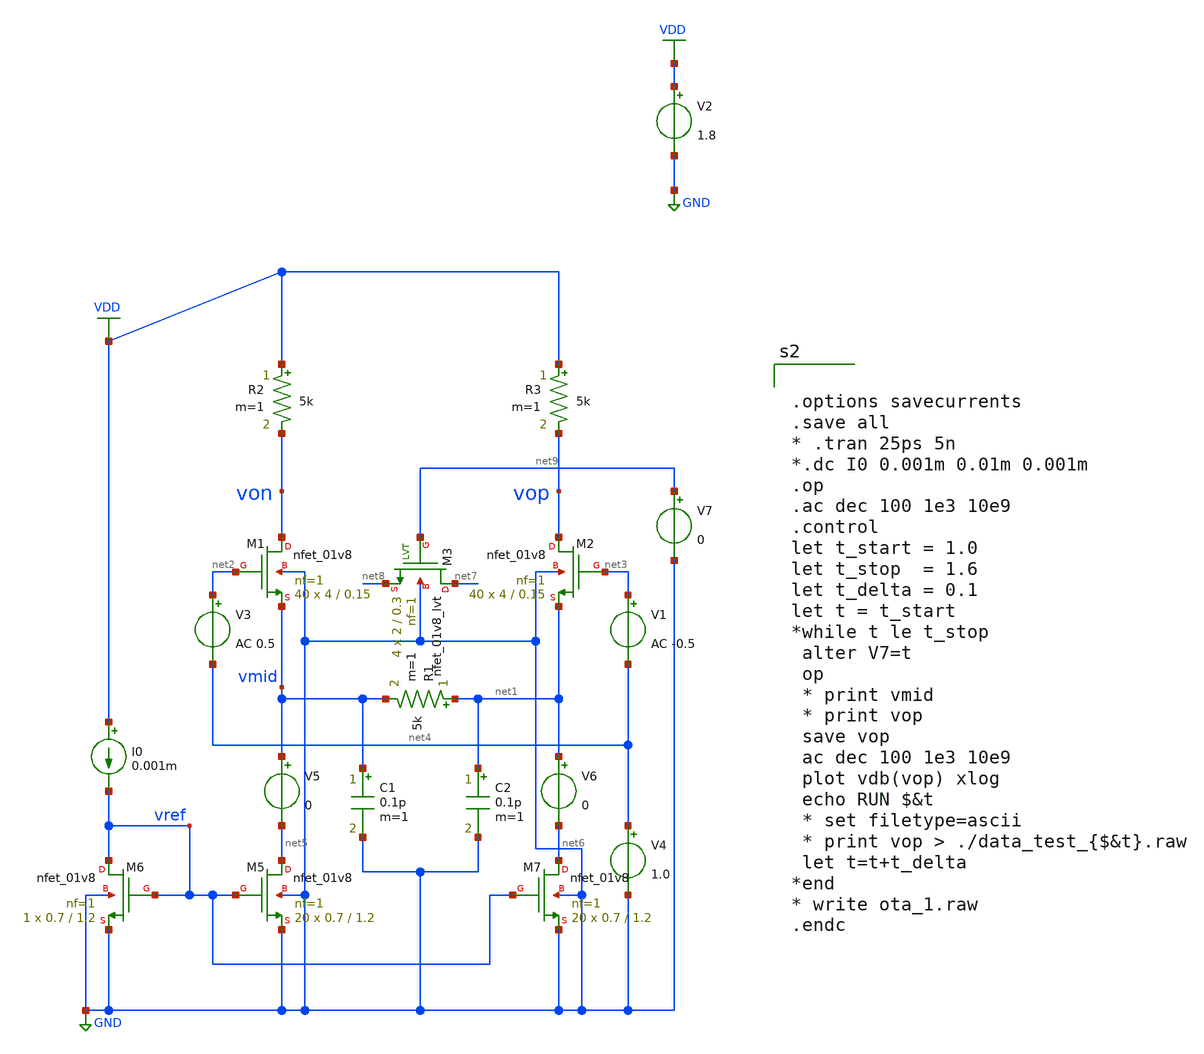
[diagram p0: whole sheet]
** sch_path: xschem/ctle_2.sch
**.subckt ctle_2
V2 VDD GND 1.8
XM5 net5 vref GND GND sky130_fd_pr__nfet_01v8 L=1.2 W=0.7 nf=1 ad='int((nf+1)/2) * W/nf * 0.29' as='int((nf+2)/2) * W/nf * 0.29'
+ pd='2*int((nf+1)/2) * (W/nf + 0.29)' ps='2*int((nf+2)/2) * (W/nf + 0.29)' nrd='0.29 / W' nrs='0.29 / W'
+ sa=0 sb=0 sd=0 mult=20 m=20
XM6 vref vref GND GND sky130_fd_pr__nfet_01v8 L=1.2 W=0.7 nf=1 ad='int((nf+1)/2) * W/nf * 0.29' as='int((nf+2)/2) * W/nf * 0.29'
+ pd='2*int((nf+1)/2) * (W/nf + 0.29)' ps='2*int((nf+2)/2) * (W/nf + 0.29)' nrd='0.29 / W' nrs='0.29 / W'
+ sa=0 sb=0 sd=0 mult=1 m=1
I0 VDD vref 0.001m
V3 net2 net4 AC 0.5
V4 net4 GND 1.0
V5 vmid net5 0
V1 net3 net4 AC -0.5
XM7 net6 vref GND GND sky130_fd_pr__nfet_01v8 L=1.2 W=0.7 nf=1 ad='int((nf+1)/2) * W/nf * 0.29' as='int((nf+2)/2) * W/nf * 0.29'
+ pd='2*int((nf+1)/2) * (W/nf + 0.29)' ps='2*int((nf+2)/2) * (W/nf + 0.29)' nrd='0.29 / W' nrs='0.29 / W'
+ sa=0 sb=0 sd=0 mult=20 m=20
V6 net1 net6 0
R1 net1 vmid 5k m=1
R2 VDD von 5k m=1
R3 VDD vop 5k m=1
C1 vmid GND 0.1p m=1
C2 net1 GND 0.1p m=1
XM3 net7 net9 net8 GND sky130_fd_pr__nfet_01v8_lvt L=0.3 W=2 nf=1 ad='int((nf+1)/2) * W/nf * 0.29' as='int((nf+2)/2) * W/nf * 0.29'
+ pd='2*int((nf+1)/2) * (W/nf + 0.29)' ps='2*int((nf+2)/2) * (W/nf + 0.29)' nrd='0.29 / W' nrs='0.29 / W'
+ sa=0 sb=0 sd=0 mult=4 m=4
V7 net9 GND 0
XM1 von net2 vmid GND sky130_fd_pr__nfet_01v8 L=0.15 W=4 nf=1 ad='int((nf+1)/2) * W/nf * 0.29' as='int((nf+2)/2) * W/nf * 0.29'
+ pd='2*int((nf+1)/2) * (W/nf + 0.29)' ps='2*int((nf+2)/2) * (W/nf + 0.29)' nrd='0.29 / W' nrs='0.29 / W'
+ sa=0 sb=0 sd=0 mult=40 m=40
XM2 vop net3 net1 GND sky130_fd_pr__nfet_01v8 L=0.15 W=4 nf=1 ad='int((nf+1)/2) * W/nf * 0.29' as='int((nf+2)/2) * W/nf * 0.29'
+ pd='2*int((nf+1)/2) * (W/nf + 0.29)' ps='2*int((nf+2)/2) * (W/nf + 0.29)' nrd='0.29 / W' nrs='0.29 / W'
+ sa=0 sb=0 sd=0 mult=40 m=40
**** begin user architecture code
.lib $::SKYWATER_MODELS/sky130.lib.spice tt
* .include $::PDKPATH/libs.ref/sky130_fd_sc_hvl/spice/sky130_fd_sc_hvl.spice



.options savecurrents
.save all
* .tran 25ps 5n
*.dc I0 0.001m 0.01m 0.001m
.op
.ac dec 100 1e3 10e9
.control
let t_start = 1.0
let t_stop  = 1.6
let t_delta = 0.1
let t = t_start
*while t le t_stop
 alter V7=t
 op
 * print vmid
 * print vop
 save vop
 ac dec 100 1e3 10e9
 plot vdb(vop) xlog
 echo RUN $&t
 * set filetype=ascii
 * print vop > ./data_test_{$&t}.raw
 let t=t+t_delta
*end
* write ota_1.raw
.endc


**** end user architecture code
**.ends
.GLOBAL VDD
.GLOBAL GND
.end
